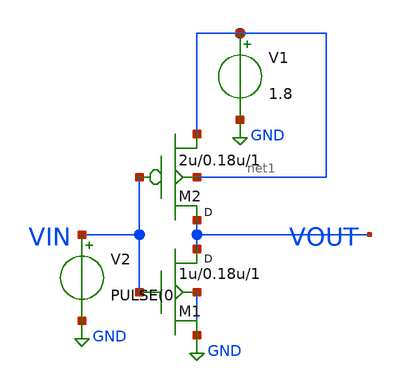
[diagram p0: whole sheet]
** sch_path: My_Inverter/inverter.sch
**.subckt inverter
M1 VOUT VIN GND GND nmos w=1u l=0.18u m=1
M2 VOUT VIN net1 net1 pmos w=2u l=0.18u m=1
V1 net1 GND 1.8
V2 VIN GND PULSE(0
**.ends
.GLOBAL GND
.end
